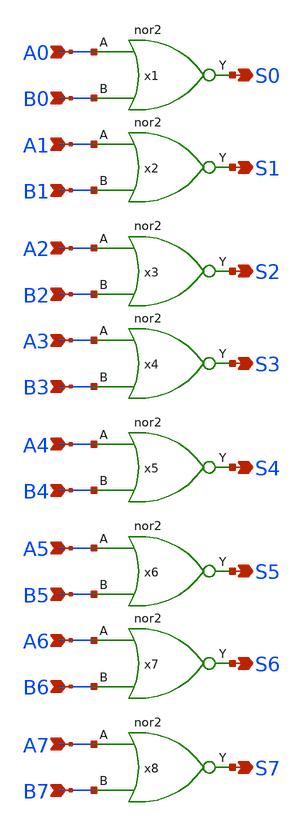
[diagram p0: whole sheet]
** sch_path: design/xschem/NOR/nor_8_bitwise.sch
**.subckt nor_8_bitwise S0 S1 S2 S3 S4 S5 S6 S7 A0 B0 A1 B1 A2 B2 A3 B3 A4 B4 A5 B5 A6 B6 A7 B7
*.opin S0
*.opin S1
*.opin S2
*.opin S3
*.opin S4
*.opin S5
*.opin S6
*.opin S7
*.ipin A0
*.ipin B0
*.ipin A1
*.ipin B1
*.ipin A2
*.ipin B2
*.ipin A3
*.ipin B3
*.ipin A4
*.ipin B4
*.ipin A5
*.ipin B5
*.ipin A6
*.ipin B6
*.ipin A7
*.ipin B7
x1 A0 B0 VSS VDD S0 nor2
x2 A1 B1 VSS VDD S1 nor2
x3 A2 B2 VSS VDD S2 nor2
x4 A3 B3 VSS VDD S3 nor2
x5 A4 B4 VSS VDD S4 nor2
x6 A5 B5 VSS VDD S5 nor2
x7 A6 B6 VSS VDD S6 nor2
x8 A7 B7 VSS VDD S7 nor2
**.ends
.end
